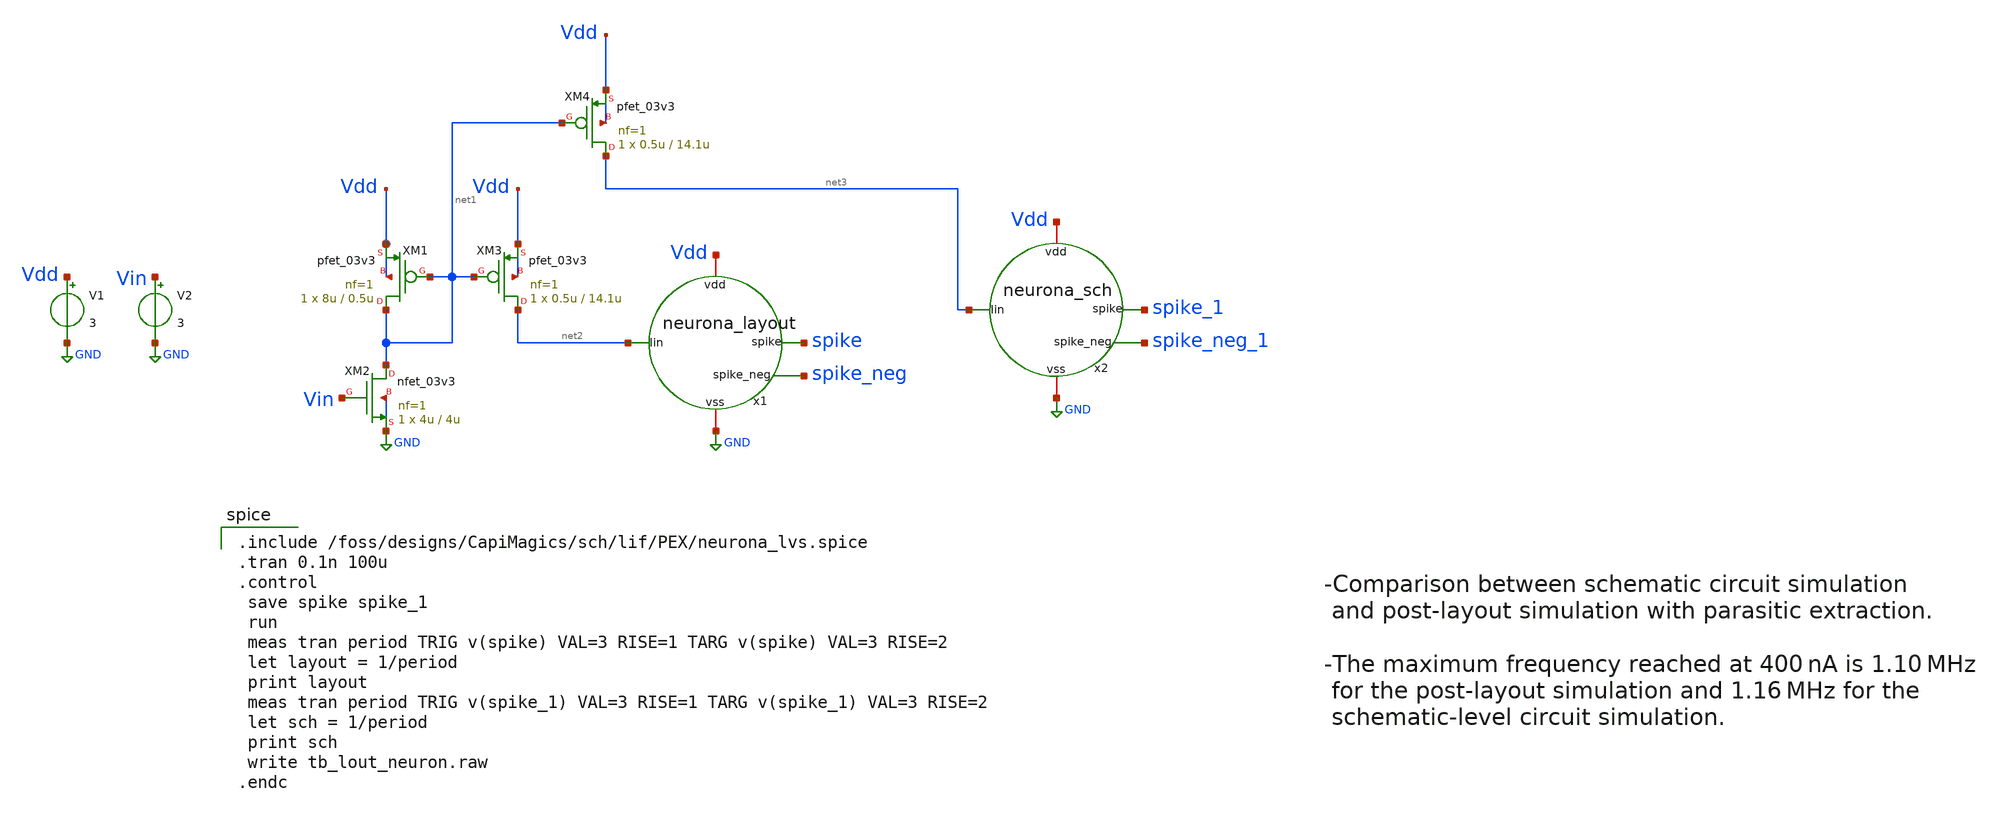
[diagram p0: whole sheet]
** sch_path: designs/libs/snn_analog/lif/sch/lif/tb_lout_neuron.sch
**.subckt tb_lout_neuron
XM1 net1 net1 Vdd Vdd pfet_03v3 L=0.5u W=8u nf=1 ad='int((nf+1)/2) * W/nf * 0.18u' as='int((nf+2)/2) * W/nf * 0.18u'
+ pd='2*int((nf+1)/2) * (W/nf + 0.18u)' ps='2*int((nf+2)/2) * (W/nf + 0.18u)' nrd='0.18u / W' nrs='0.18u / W'
+ sa=0 sb=0 sd=0 m=1
XM2 net1 Vin GND GND nfet_03v3 L=4u W=4u nf=1 ad='int((nf+1)/2) * W/nf * 0.18u' as='int((nf+2)/2) * W/nf * 0.18u'
+ pd='2*int((nf+1)/2) * (W/nf + 0.18u)' ps='2*int((nf+2)/2) * (W/nf + 0.18u)' nrd='0.18u / W' nrs='0.18u / W'
+ sa=0 sb=0 sd=0 m=1
XM3 net2 net1 Vdd Vdd pfet_03v3 L=14.1u W=0.5u nf=1 ad='int((nf+1)/2) * W/nf * 0.18u' as='int((nf+2)/2) * W/nf * 0.18u'
+ pd='2*int((nf+1)/2) * (W/nf + 0.18u)' ps='2*int((nf+2)/2) * (W/nf + 0.18u)' nrd='0.18u / W' nrs='0.18u / W'
+ sa=0 sb=0 sd=0 m=1
V1 Vdd GND 3
V2 Vin GND 3
x1 net2 Vdd GND spike spike_neg neurona_layout
x2 net3 Vdd GND spike_1 spike_neg_1 neurona_sch
XM4 net3 net1 Vdd Vdd pfet_03v3 L=14.1u W=0.5u nf=1 ad='int((nf+1)/2) * W/nf * 0.18u' as='int((nf+2)/2) * W/nf * 0.18u'
+ pd='2*int((nf+1)/2) * (W/nf + 0.18u)' ps='2*int((nf+2)/2) * (W/nf + 0.18u)' nrd='0.18u / W' nrs='0.18u / W'
+ sa=0 sb=0 sd=0 m=1
**** begin user architecture code

.include /foss/designs/CapiMagics/sch/lif/PEX/neurona_lvs.spice
.tran 0.1n 100u
.control
 save spike spike_1
 run
 meas tran period TRIG v(spike) VAL=3 RISE=1 TARG v(spike) VAL=3 RISE=2
 let layout = 1/period
 print layout
 meas tran period TRIG v(spike_1) VAL=3 RISE=1 TARG v(spike_1) VAL=3 RISE=2
 let sch = 1/period
 print sch
 write tb_lout_neuron.raw
.endc


.include $::180MCU_MODELS/design.ngspice
.lib $::180MCU_MODELS/sm141064.ngspice typical
.lib $::180MCU_MODELS/sm141064.ngspice cap_mim
.lib $::180MCU_MODELS/sm141064.ngspice res_typical
.lib $::180MCU_MODELS/sm141064.ngspice moscap_typical
.lib $::180MCU_MODELS/sm141064.ngspice mimcap_typical
* .lib $::180MCU_MODELS/sm141064.ngspice res_statistical

**** end user architecture code
**.ends
.GLOBAL GND
.end
